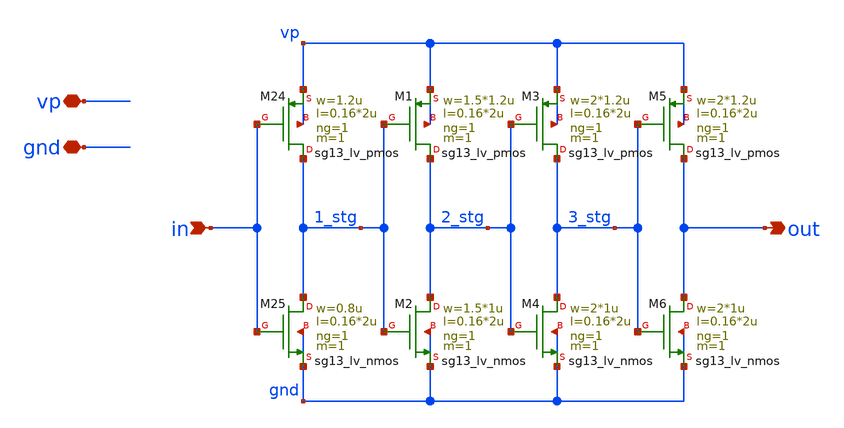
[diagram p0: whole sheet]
** sch_path: schematics/vco/vco_cell/0_buf.sch
**.subckt 0_buf in out vp gnd
*.ipin in
*.opin out
*.iopin vp
*.iopin gnd
XM24 1_stg in vp vp sg13_lv_pmos w=1.2u l=0.16*2u ng=1 m=1 mm_ok=1
XM25 1_stg in gnd gnd sg13_lv_nmos w=0.8u l=0.16*2u ng=1 m=1 mm_ok=1
XM1 2_stg 1_stg vp vp sg13_lv_pmos w=1.5*1.2u l=0.16*2u ng=1 m=1 mm_ok=1
XM2 2_stg 1_stg gnd gnd sg13_lv_nmos w=1.5*1u l=0.16*2u ng=1 m=1 mm_ok=1
XM3 3_stg 2_stg vp vp sg13_lv_pmos w=2*1.2u l=0.16*2u ng=1 m=1 mm_ok=1
XM4 3_stg 2_stg gnd gnd sg13_lv_nmos w=2*1u l=0.16*2u ng=1 m=1 mm_ok=1
XM5 out 3_stg vp vp sg13_lv_pmos w=2*1.2u l=0.16*2u ng=1 m=1 mm_ok=1
XM6 out 3_stg gnd gnd sg13_lv_nmos w=2*1u l=0.16*2u ng=1 m=1 mm_ok=1
**.ends
.end
